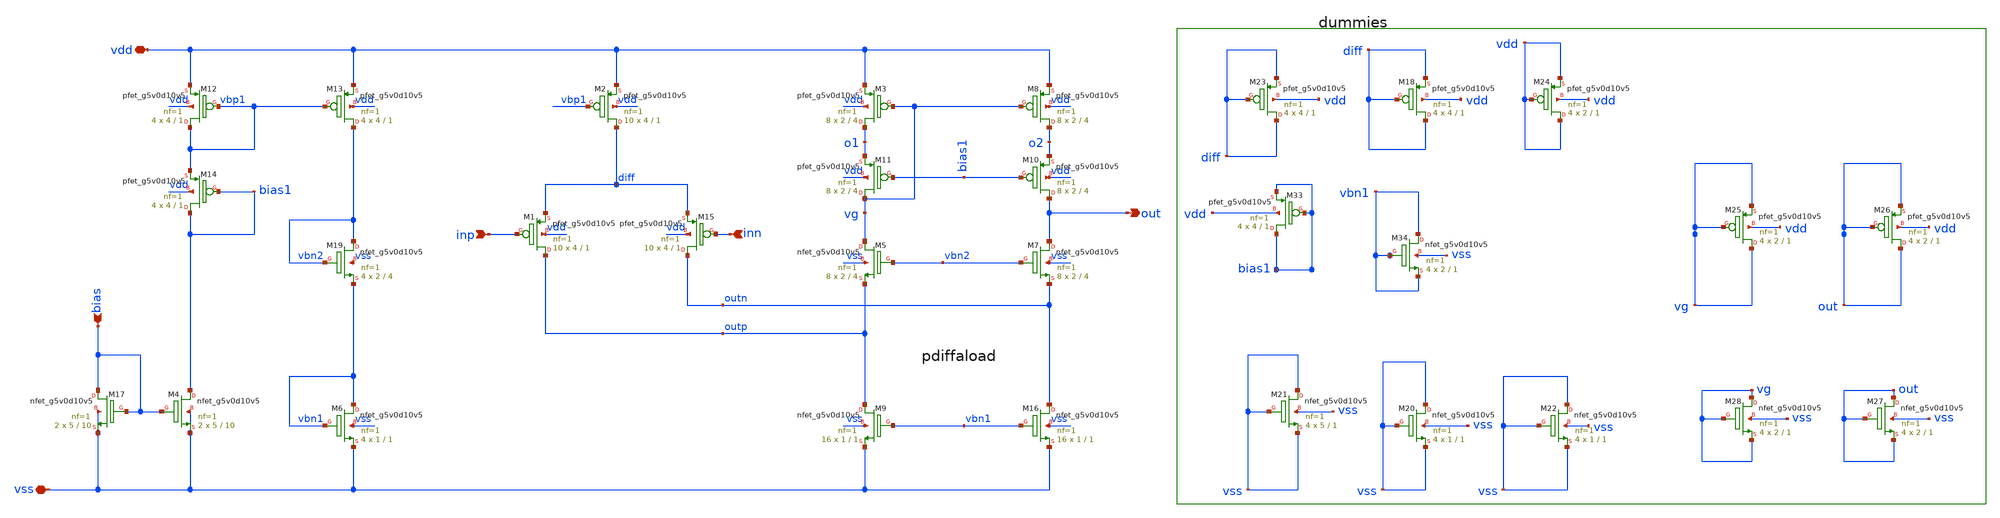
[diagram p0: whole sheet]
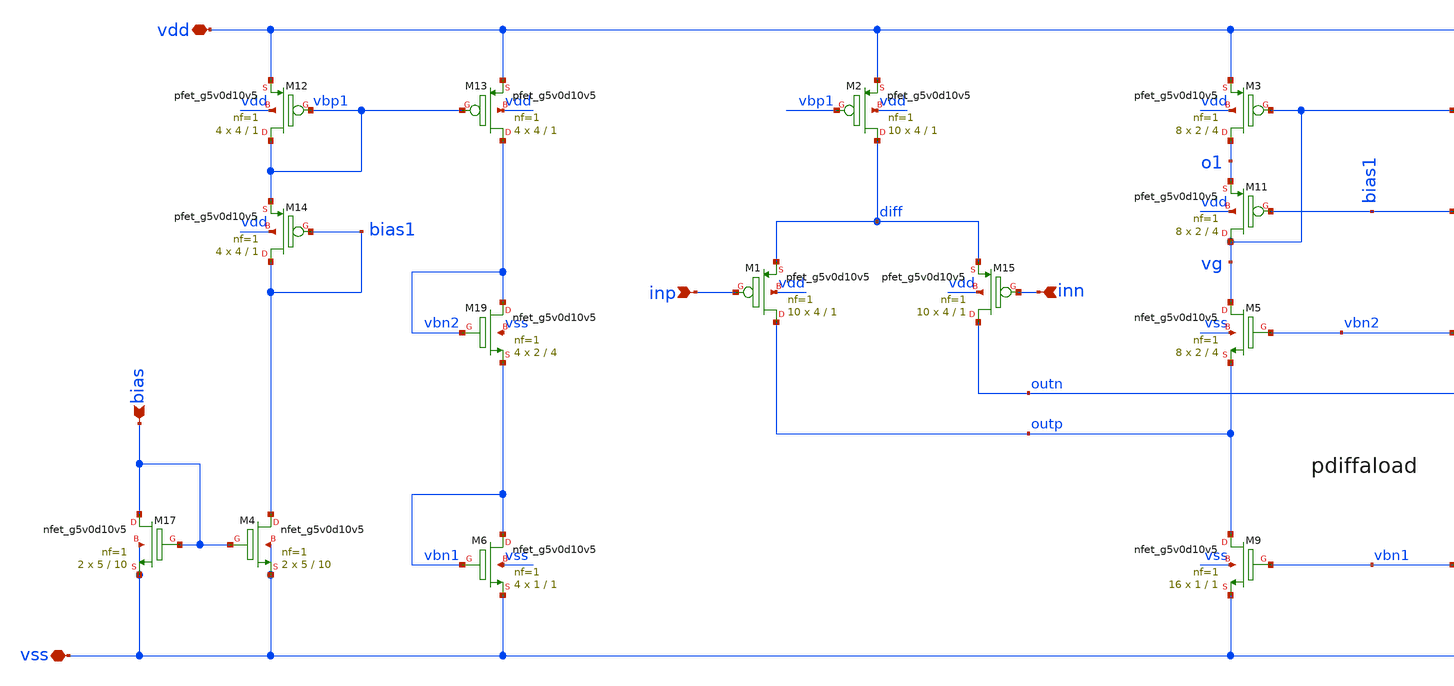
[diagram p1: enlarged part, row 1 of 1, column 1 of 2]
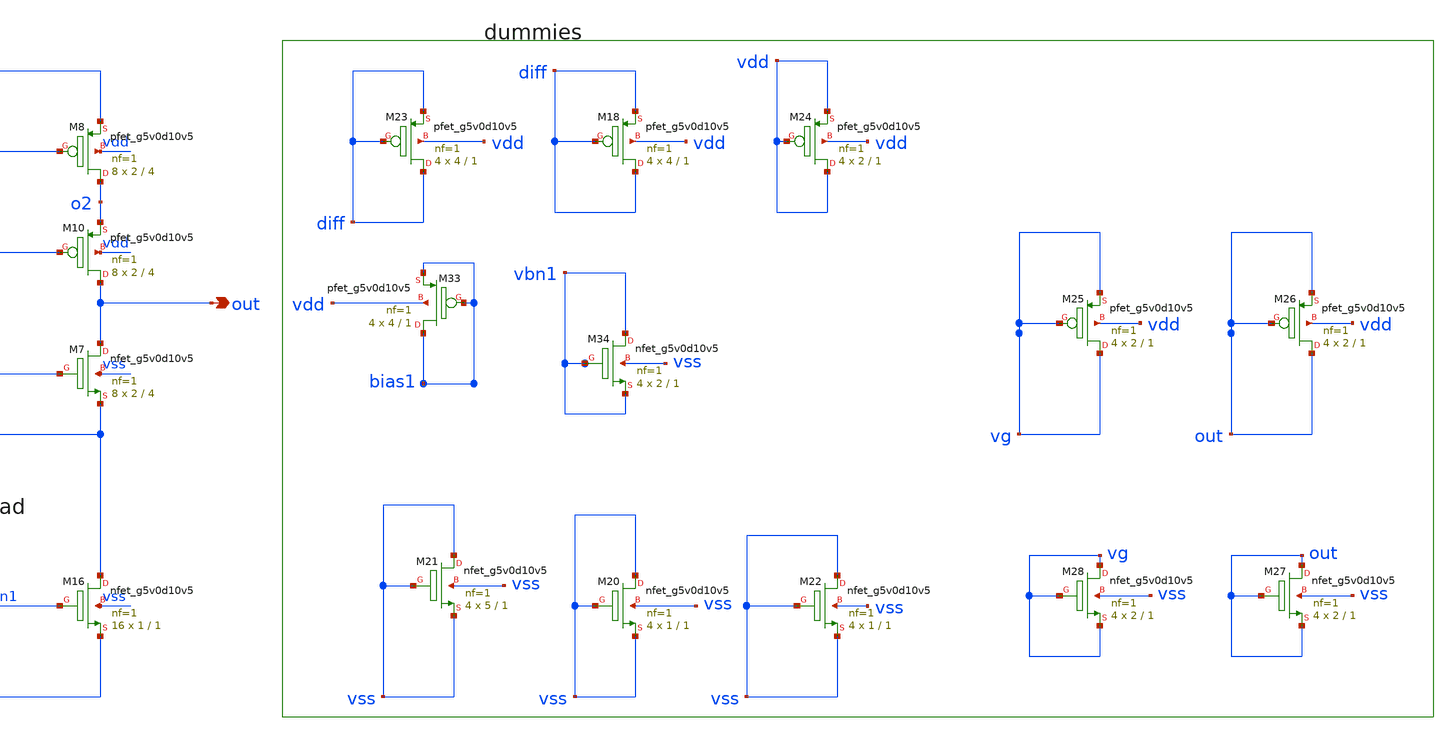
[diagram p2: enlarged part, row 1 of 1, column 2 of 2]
** sch_path: schematic/bandgapxd/ota.sch
**.subckt ota inn inp out bias vss vdd
*.ipin inn
*.ipin inp
*.opin out
*.ipin bias
*.iopin vss
*.iopin vdd
XM12 vbp1 vbp1 vdd vdd sky130_fd_pr__pfet_g5v0d10v5 L=1 W=4 nf=1 ad='int((nf+1)/2) * W/nf * 0.29' as='int((nf+2)/2) * W/nf * 0.29'
+ pd='2*int((nf+1)/2) * (W/nf + 0.29)' ps='2*int((nf+2)/2) * (W/nf + 0.29)' nrd='0.29 / W' nrs='0.29 / W'
+ sa=0 sb=0 sd=0 mult=4 m=4
XM13 vbn2 vbp1 vdd vdd sky130_fd_pr__pfet_g5v0d10v5 L=1 W=4 nf=1 ad='int((nf+1)/2) * W/nf * 0.29' as='int((nf+2)/2) * W/nf * 0.29'
+ pd='2*int((nf+1)/2) * (W/nf + 0.29)' ps='2*int((nf+2)/2) * (W/nf + 0.29)' nrd='0.29 / W' nrs='0.29 / W'
+ sa=0 sb=0 sd=0 mult=4 m=4
XM14 bias1 bias1 vbp1 vdd sky130_fd_pr__pfet_g5v0d10v5 L=1 W=4 nf=1 ad='int((nf+1)/2) * W/nf * 0.29'
+ as='int((nf+2)/2) * W/nf * 0.29' pd='2*int((nf+1)/2) * (W/nf + 0.29)' ps='2*int((nf+2)/2) * (W/nf + 0.29)'
+ nrd='0.29 / W' nrs='0.29 / W' sa=0 sb=0 sd=0 mult=4 m=4
XM1 outp inp diff vdd sky130_fd_pr__pfet_g5v0d10v5 L=1 W=4 nf=1 ad='int((nf+1)/2) * W/nf * 0.29' as='int((nf+2)/2) * W/nf * 0.29'
+ pd='2*int((nf+1)/2) * (W/nf + 0.29)' ps='2*int((nf+2)/2) * (W/nf + 0.29)' nrd='0.29 / W' nrs='0.29 / W'
+ sa=0 sb=0 sd=0 mult=10 m=10
XM2 diff vbp1 vdd vdd sky130_fd_pr__pfet_g5v0d10v5 L=1 W=4 nf=1 ad='int((nf+1)/2) * W/nf * 0.29' as='int((nf+2)/2) * W/nf * 0.29'
+ pd='2*int((nf+1)/2) * (W/nf + 0.29)' ps='2*int((nf+2)/2) * (W/nf + 0.29)' nrd='0.29 / W' nrs='0.29 / W'
+ sa=0 sb=0 sd=0 mult=10 m=10
XM3 o1 vg vdd vdd sky130_fd_pr__pfet_g5v0d10v5 L=4 W=2 nf=1 ad='int((nf+1)/2) * W/nf * 0.29' as='int((nf+2)/2) * W/nf * 0.29'
+ pd='2*int((nf+1)/2) * (W/nf + 0.29)' ps='2*int((nf+2)/2) * (W/nf + 0.29)' nrd='0.29 / W' nrs='0.29 / W'
+ sa=0 sb=0 sd=0 mult=8 m=8
XM8 o2 vg vdd vdd sky130_fd_pr__pfet_g5v0d10v5 L=4 W=2 nf=1 ad='int((nf+1)/2) * W/nf * 0.29' as='int((nf+2)/2) * W/nf * 0.29'
+ pd='2*int((nf+1)/2) * (W/nf + 0.29)' ps='2*int((nf+2)/2) * (W/nf + 0.29)' nrd='0.29 / W' nrs='0.29 / W'
+ sa=0 sb=0 sd=0 mult=8 m=8
XM10 out bias1 o2 vdd sky130_fd_pr__pfet_g5v0d10v5 L=4 W=2 nf=1 ad='int((nf+1)/2) * W/nf * 0.29' as='int((nf+2)/2) * W/nf * 0.29'
+ pd='2*int((nf+1)/2) * (W/nf + 0.29)' ps='2*int((nf+2)/2) * (W/nf + 0.29)' nrd='0.29 / W' nrs='0.29 / W'
+ sa=0 sb=0 sd=0 mult=8 m=8
XM11 vg bias1 o1 vdd sky130_fd_pr__pfet_g5v0d10v5 L=4 W=2 nf=1 ad='int((nf+1)/2) * W/nf * 0.29' as='int((nf+2)/2) * W/nf * 0.29'
+ pd='2*int((nf+1)/2) * (W/nf + 0.29)' ps='2*int((nf+2)/2) * (W/nf + 0.29)' nrd='0.29 / W' nrs='0.29 / W'
+ sa=0 sb=0 sd=0 mult=8 m=8
XM19 vbn2 vbn2 vbn1 vss sky130_fd_pr__nfet_g5v0d10v5 L=4 W=2 nf=1 ad='int((nf+1)/2) * W/nf * 0.29' as='int((nf+2)/2) * W/nf * 0.29'
+ pd='2*int((nf+1)/2) * (W/nf + 0.29)' ps='2*int((nf+2)/2) * (W/nf + 0.29)' nrd='0.29 / W' nrs='0.29 / W'
+ sa=0 sb=0 sd=0 mult=4 m=4
XM5 vg vbn2 outp vss sky130_fd_pr__nfet_g5v0d10v5 L=4 W=2 nf=1 ad='int((nf+1)/2) * W/nf * 0.29' as='int((nf+2)/2) * W/nf * 0.29'
+ pd='2*int((nf+1)/2) * (W/nf + 0.29)' ps='2*int((nf+2)/2) * (W/nf + 0.29)' nrd='0.29 / W' nrs='0.29 / W'
+ sa=0 sb=0 sd=0 mult=8 m=8
XM9 outp vbn1 vss vss sky130_fd_pr__nfet_g5v0d10v5 L=1 W=1 nf=1 ad='int((nf+1)/2) * W/nf * 0.29' as='int((nf+2)/2) * W/nf * 0.29'
+ pd='2*int((nf+1)/2) * (W/nf + 0.29)' ps='2*int((nf+2)/2) * (W/nf + 0.29)' nrd='0.29 / W' nrs='0.29 / W'
+ sa=0 sb=0 sd=0 mult=16 m=16
XM16 outn vbn1 vss vss sky130_fd_pr__nfet_g5v0d10v5 L=1 W=1 nf=1 ad='int((nf+1)/2) * W/nf * 0.29' as='int((nf+2)/2) * W/nf * 0.29'
+ pd='2*int((nf+1)/2) * (W/nf + 0.29)' ps='2*int((nf+2)/2) * (W/nf + 0.29)' nrd='0.29 / W' nrs='0.29 / W'
+ sa=0 sb=0 sd=0 mult=16 m=16
XM7 out vbn2 outn vss sky130_fd_pr__nfet_g5v0d10v5 L=4 W=2 nf=1 ad='int((nf+1)/2) * W/nf * 0.29' as='int((nf+2)/2) * W/nf * 0.29'
+ pd='2*int((nf+1)/2) * (W/nf + 0.29)' ps='2*int((nf+2)/2) * (W/nf + 0.29)' nrd='0.29 / W' nrs='0.29 / W'
+ sa=0 sb=0 sd=0 mult=8 m=8
XM6 vbn1 vbn1 vss vss sky130_fd_pr__nfet_g5v0d10v5 L=1 W=1 nf=1 ad='int((nf+1)/2) * W/nf * 0.29' as='int((nf+2)/2) * W/nf * 0.29'
+ pd='2*int((nf+1)/2) * (W/nf + 0.29)' ps='2*int((nf+2)/2) * (W/nf + 0.29)' nrd='0.29 / W' nrs='0.29 / W'
+ sa=0 sb=0 sd=0 mult=4 m=4
XM15 outn inn diff vdd sky130_fd_pr__pfet_g5v0d10v5 L=1 W=4 nf=1 ad='int((nf+1)/2) * W/nf * 0.29' as='int((nf+2)/2) * W/nf * 0.29'
+ pd='2*int((nf+1)/2) * (W/nf + 0.29)' ps='2*int((nf+2)/2) * (W/nf + 0.29)' nrd='0.29 / W' nrs='0.29 / W'
+ sa=0 sb=0 sd=0 mult=10 m=10
XM4 bias1 bias vss vss sky130_fd_pr__nfet_g5v0d10v5 L=10 W=5 nf=1 ad='int((nf+1)/2) * W/nf * 0.29' as='int((nf+2)/2) * W/nf * 0.29'
+ pd='2*int((nf+1)/2) * (W/nf + 0.29)' ps='2*int((nf+2)/2) * (W/nf + 0.29)' nrd='0.29 / W' nrs='0.29 / W'
+ sa=0 sb=0 sd=0 mult=2 m=2
XM17 bias bias vss vss sky130_fd_pr__nfet_g5v0d10v5 L=10 W=5 nf=1 ad='int((nf+1)/2) * W/nf * 0.29' as='int((nf+2)/2) * W/nf * 0.29'
+ pd='2*int((nf+1)/2) * (W/nf + 0.29)' ps='2*int((nf+2)/2) * (W/nf + 0.29)' nrd='0.29 / W' nrs='0.29 / W'
+ sa=0 sb=0 sd=0 mult=2 m=2
XM18 diff diff diff vdd sky130_fd_pr__pfet_g5v0d10v5 L=1 W=4 nf=1 ad='int((nf+1)/2) * W/nf * 0.29' as='int((nf+2)/2) * W/nf * 0.29'
+ pd='2*int((nf+1)/2) * (W/nf + 0.29)' ps='2*int((nf+2)/2) * (W/nf + 0.29)' nrd='0.29 / W' nrs='0.29 / W'
+ sa=0 sb=0 sd=0 mult=4 m=4
XM20 vss vss vss vss sky130_fd_pr__nfet_g5v0d10v5 L=1 W=1 nf=1 ad='int((nf+1)/2) * W/nf * 0.29' as='int((nf+2)/2) * W/nf * 0.29'
+ pd='2*int((nf+1)/2) * (W/nf + 0.29)' ps='2*int((nf+2)/2) * (W/nf + 0.29)' nrd='0.29 / W' nrs='0.29 / W'
+ sa=0 sb=0 sd=0 mult=4 m=4
XM21 vss vss vss vss sky130_fd_pr__nfet_g5v0d10v5 L=1 W=5 nf=1 ad='int((nf+1)/2) * W/nf * 0.29' as='int((nf+2)/2) * W/nf * 0.29'
+ pd='2*int((nf+1)/2) * (W/nf + 0.29)' ps='2*int((nf+2)/2) * (W/nf + 0.29)' nrd='0.29 / W' nrs='0.29 / W'
+ sa=0 sb=0 sd=0 mult=4 m=4
XM22 vss vss vss vss sky130_fd_pr__nfet_g5v0d10v5 L=1 W=1 nf=1 ad='int((nf+1)/2) * W/nf * 0.29' as='int((nf+2)/2) * W/nf * 0.29'
+ pd='2*int((nf+1)/2) * (W/nf + 0.29)' ps='2*int((nf+2)/2) * (W/nf + 0.29)' nrd='0.29 / W' nrs='0.29 / W'
+ sa=0 sb=0 sd=0 mult=4 m=4
XM23 diff diff diff vdd sky130_fd_pr__pfet_g5v0d10v5 L=1 W=4 nf=1 ad='int((nf+1)/2) * W/nf * 0.29' as='int((nf+2)/2) * W/nf * 0.29'
+ pd='2*int((nf+1)/2) * (W/nf + 0.29)' ps='2*int((nf+2)/2) * (W/nf + 0.29)' nrd='0.29 / W' nrs='0.29 / W'
+ sa=0 sb=0 sd=0 mult=4 m=4
XM24 vdd vdd vdd vdd sky130_fd_pr__pfet_g5v0d10v5 L=1 W=2 nf=1 ad='int((nf+1)/2) * W/nf * 0.29' as='int((nf+2)/2) * W/nf * 0.29'
+ pd='2*int((nf+1)/2) * (W/nf + 0.29)' ps='2*int((nf+2)/2) * (W/nf + 0.29)' nrd='0.29 / W' nrs='0.29 / W'
+ sa=0 sb=0 sd=0 mult=4 m=4
XM34 vbn1 vbn1 vbn1 vss sky130_fd_pr__nfet_g5v0d10v5 L=1 W=2 nf=1 ad='int((nf+1)/2) * W/nf * 0.29' as='int((nf+2)/2) * W/nf * 0.29'
+ pd='2*int((nf+1)/2) * (W/nf + 0.29)' ps='2*int((nf+2)/2) * (W/nf + 0.29)' nrd='0.29 / W' nrs='0.29 / W'
+ sa=0 sb=0 sd=0 mult=4 m=4
XM33 bias1 bias1 bias1 vdd sky130_fd_pr__pfet_g5v0d10v5 L=1 W=4 nf=1 ad='int((nf+1)/2) * W/nf * 0.29'
+ as='int((nf+2)/2) * W/nf * 0.29' pd='2*int((nf+1)/2) * (W/nf + 0.29)' ps='2*int((nf+2)/2) * (W/nf + 0.29)'
+ nrd='0.29 / W' nrs='0.29 / W' sa=0 sb=0 sd=0 mult=4 m=4
XM25 vg vg vg vdd sky130_fd_pr__pfet_g5v0d10v5 L=1 W=2 nf=1 ad='int((nf+1)/2) * W/nf * 0.29' as='int((nf+2)/2) * W/nf * 0.29'
+ pd='2*int((nf+1)/2) * (W/nf + 0.29)' ps='2*int((nf+2)/2) * (W/nf + 0.29)' nrd='0.29 / W' nrs='0.29 / W'
+ sa=0 sb=0 sd=0 mult=4 m=4
XM26 out out out vdd sky130_fd_pr__pfet_g5v0d10v5 L=1 W=2 nf=1 ad='int((nf+1)/2) * W/nf * 0.29' as='int((nf+2)/2) * W/nf * 0.29'
+ pd='2*int((nf+1)/2) * (W/nf + 0.29)' ps='2*int((nf+2)/2) * (W/nf + 0.29)' nrd='0.29 / W' nrs='0.29 / W'
+ sa=0 sb=0 sd=0 mult=4 m=4
XM27 out out out vss sky130_fd_pr__nfet_g5v0d10v5 L=1 W=2 nf=1 ad='int((nf+1)/2) * W/nf * 0.29' as='int((nf+2)/2) * W/nf * 0.29'
+ pd='2*int((nf+1)/2) * (W/nf + 0.29)' ps='2*int((nf+2)/2) * (W/nf + 0.29)' nrd='0.29 / W' nrs='0.29 / W'
+ sa=0 sb=0 sd=0 mult=4 m=4
XM28 vg vg vg vss sky130_fd_pr__nfet_g5v0d10v5 L=1 W=2 nf=1 ad='int((nf+1)/2) * W/nf * 0.29' as='int((nf+2)/2) * W/nf * 0.29'
+ pd='2*int((nf+1)/2) * (W/nf + 0.29)' ps='2*int((nf+2)/2) * (W/nf + 0.29)' nrd='0.29 / W' nrs='0.29 / W'
+ sa=0 sb=0 sd=0 mult=4 m=4
**.ends
.end
